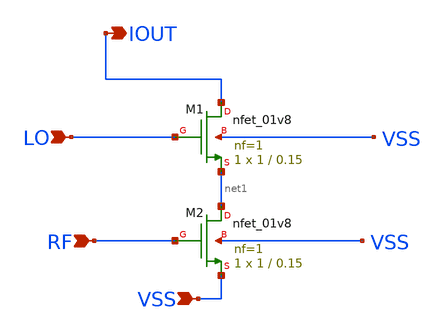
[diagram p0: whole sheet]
** sch_path: mixer.sch
**.subckt mixer VSS IOUT LO RF
*.ipin VSS
*.opin IOUT
*.ipin LO
*.ipin RF
XM1 IOUT LO net1 VSS sky130_fd_pr__nfet_01v8 L=0.15 W=1 nf=1 ad='int((nf+1)/2) * W/nf * 0.29' as='int((nf+2)/2) * W/nf * 0.29'
+ pd='2*int((nf+1)/2) * (W/nf + 0.29)' ps='2*int((nf+2)/2) * (W/nf + 0.29)' nrd='0.29 / W' nrs='0.29 / W'
+ sa=0 sb=0 sd=0 mult=1 m=1
XM2 net1 RF VSS VSS sky130_fd_pr__nfet_01v8 L=0.15 W=1 nf=1 ad='int((nf+1)/2) * W/nf * 0.29' as='int((nf+2)/2) * W/nf * 0.29'
+ pd='2*int((nf+1)/2) * (W/nf + 0.29)' ps='2*int((nf+2)/2) * (W/nf + 0.29)' nrd='0.29 / W' nrs='0.29 / W'
+ sa=0 sb=0 sd=0 mult=1 m=1
**.ends
.end
